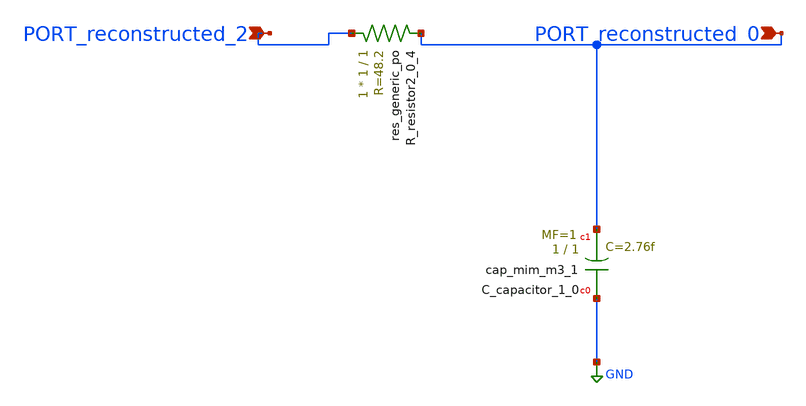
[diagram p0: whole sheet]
** sch_path: schematics/AMSNet/776.sch
**.subckt 776 PORT_reconstructed_0 PORT_reconstructed_2
*.ipin PORT_reconstructed_0
*.ipin PORT_reconstructed_2
XC_capacitor_1_0 GND PORT_reconstructed_0 sky130_fd_pr__cap_mim_m3_1 W=1 L=1 MF=1 m=1
XR_resistor2_0_4 PORT_reconstructed_2 PORT_reconstructed_0 sky130_fd_pr__res_generic_po W=1 L=1 m=1
**.ends
.GLOBAL GND
.end
